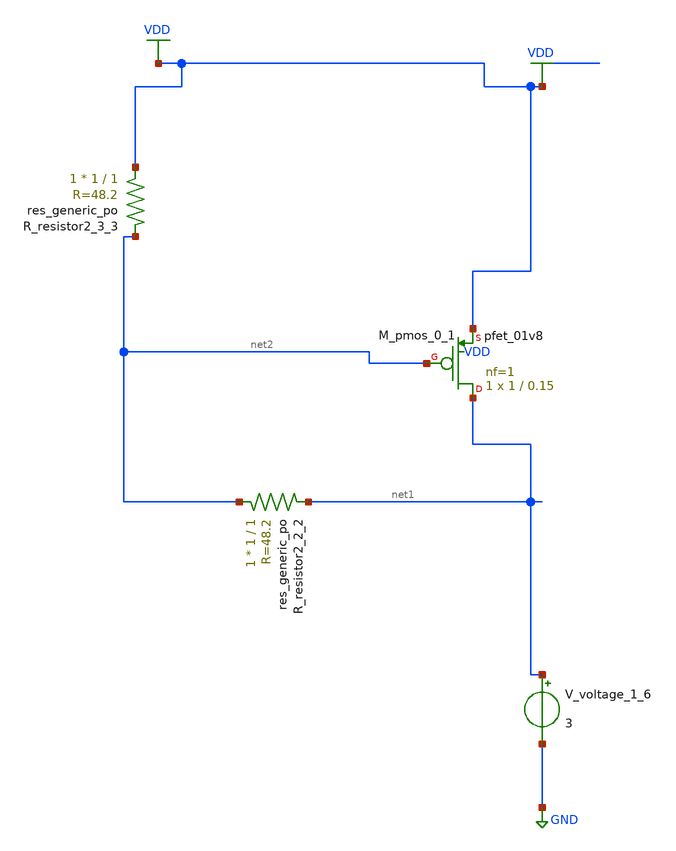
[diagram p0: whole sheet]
** sch_path: schematics/AMSNet/160.sch
**.subckt 160
XM_pmos_0_1 net1 net2 VDD VDD sky130_fd_pr__pfet_01v8 L=0.15 W=1 nf=1 ad='int((1 + 1)/2) * 1 / 1 * 0.29'
+ as='int((1 + 2)/2) * 1 / 1 * 0.29' pd='2*int((1 + 1)/2) * (1 / 1 + 0.29)' ps='2*int((1 + 2)/2) * (1 / 1 + 0.29)'
+ nrd='0.29 / 1 ' nrs='0.29 / 1 ' sa=0 sb=0 sd=0 mult=1 m=1
XR_resistor2_2_2 net2 net1 sky130_fd_pr__res_generic_po W=1 L=1 m=1
XR_resistor2_3_3 VDD net2 sky130_fd_pr__res_generic_po W=1 L=1 m=1
V_voltage_1_6 net1 GND 3
**.ends
.GLOBAL GND
.GLOBAL VDD
.end
